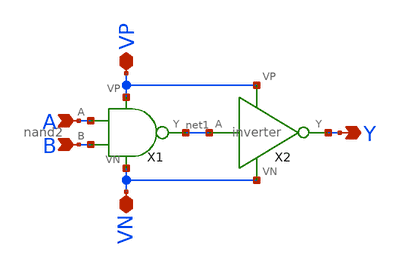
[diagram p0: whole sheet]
** sch_path: schematic/and2.sch
**.subckt and2 VP VN A B Y
*.iopin VP
*.iopin VN
*.ipin A
*.ipin B
*.opin Y
X1 A B net1 VP VN nand2
X2 net1 Y VP VN inverter
**.ends

* expanding   symbol:  /home/madvlsi/Documents/MADVLSI-Final_Project/schematic/nand2.sym # of pins=5
** sym_path: schematic/nand2.sym
** sch_path: schematic/nand2.sch
.subckt nand2 A B Y VP VN
*.ipin A
*.opin Y
*.ipin B
*.iopin VP
*.iopin VP
*.iopin VN
*.iopin VN
XM1 Y A VP VP sky130_fd_pr__pfet_01v8 L=0.15 W=2 nf=1 ad='int((nf+1)/2) * W/nf * 0.29' as='int((nf+2)/2) * W/nf * 0.29'
+ pd='2*int((nf+1)/2) * (W/nf + 0.29)' ps='2*int((nf+2)/2) * (W/nf + 0.29)' nrd='0.29 / W' nrs='0.29 / W'
+ sa=0 sb=0 sd=0 mult=1 m=1
XM2 VP B Y VP sky130_fd_pr__pfet_01v8 L=0.15 W=2 nf=1 ad='int((nf+1)/2) * W/nf * 0.29' as='int((nf+2)/2) * W/nf * 0.29'
+ pd='2*int((nf+1)/2) * (W/nf + 0.29)' ps='2*int((nf+2)/2) * (W/nf + 0.29)' nrd='0.29 / W' nrs='0.29 / W'
+ sa=0 sb=0 sd=0 mult=1 m=1
XM3 net1 B Y VN sky130_fd_pr__nfet_01v8 L=0.15 W=2 nf=1 ad='int((nf+1)/2) * W/nf * 0.29' as='int((nf+2)/2) * W/nf * 0.29'
+ pd='2*int((nf+1)/2) * (W/nf + 0.29)' ps='2*int((nf+2)/2) * (W/nf + 0.29)' nrd='0.29 / W' nrs='0.29 / W'
+ sa=0 sb=0 sd=0 mult=1 m=1
XM4 net1 A VN VN sky130_fd_pr__nfet_01v8 L=0.15 W=2 nf=1 ad='int((nf+1)/2) * W/nf * 0.29' as='int((nf+2)/2) * W/nf * 0.29'
+ pd='2*int((nf+1)/2) * (W/nf + 0.29)' ps='2*int((nf+2)/2) * (W/nf + 0.29)' nrd='0.29 / W' nrs='0.29 / W'
+ sa=0 sb=0 sd=0 mult=1 m=1
.ends


* expanding   symbol:  /home/madvlsi/Documents/MADVLSI-Final_Project/schematic/inverter.sym # of
*+ pins=4
** sym_path: schematic/inverter.sym
** sch_path: schematic/inverter.sch
.subckt inverter A Y VP VN
*.opin Y
*.ipin A
*.iopin VP
*.iopin VN
XM3 Y A VP VDD sky130_fd_pr__pfet_01v8 L={Lp} W={Wp} nf=1 ad='int((nf+1)/2) * W/nf * 0.29' as='int((nf+2)/2) * W/nf * 0.29'
+ pd='2*int((nf+1)/2) * (W/nf + 0.29)' ps='2*int((nf+2)/2) * (W/nf + 0.29)' nrd='0.29 / W' nrs='0.29 / W'
+ sa=0 sb=0 sd=0 mult=1 m=1
XM4 Y A VP VDD sky130_fd_pr__pfet_01v8 L={Lp} W={Wp} nf=1 ad='int((nf+1)/2) * W/nf * 0.29' as='int((nf+2)/2) * W/nf * 0.29'
+ pd='2*int((nf+1)/2) * (W/nf + 0.29)' ps='2*int((nf+2)/2) * (W/nf + 0.29)' nrd='0.29 / W' nrs='0.29 / W'
+ sa=0 sb=0 sd=0 mult=1 m=1
XM5 Y A VN GND sky130_fd_pr__nfet_01v8 L={Lp} W={Wp} nf=1 ad='int((nf+1)/2) * W/nf * 0.29' as='int((nf+2)/2) * W/nf * 0.29'
+ pd='2*int((nf+1)/2) * (W/nf + 0.29)' ps='2*int((nf+2)/2) * (W/nf + 0.29)' nrd='0.29 / W' nrs='0.29 / W'
+ sa=0 sb=0 sd=0 mult=1 m=1
.ends

.end
